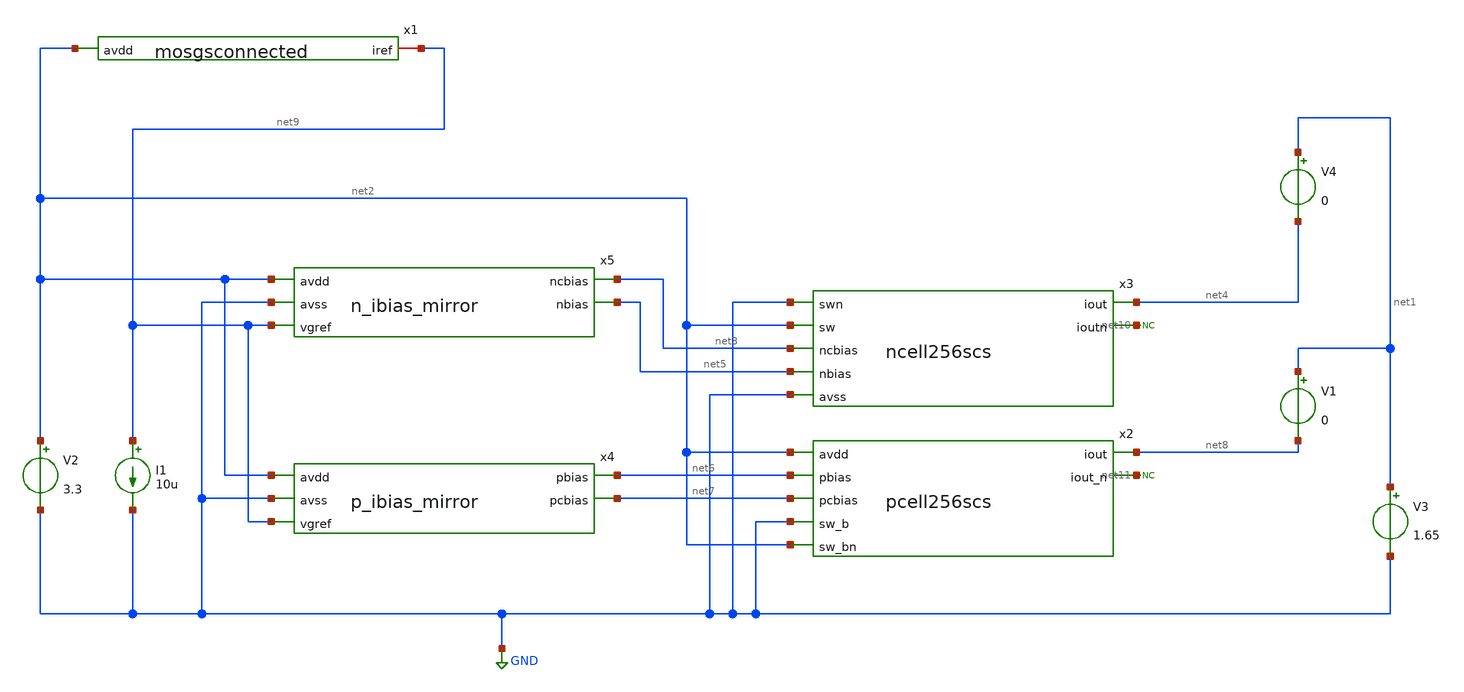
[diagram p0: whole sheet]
** sch_path: xschem/currentmirrors_tb.sch
**.subckt currentmirrors_tb
V2 net2 GND 3.3
V3 net1 GND 1.65
V4 net1 net4 0
I1 net9 GND 10u
V1 net1 net8 0
* noconn #net10
* noconn #net11
x1 net2 net9 mosgsconnected
x4 net2 net6 net9 net7 GND p_ibias_mirror
x5 net2 net9 net3 net5 GND n_ibias_mirror
x2 net2 net6 net7 GND net2 net11 net8 pcell256scs
x3 net4 net10 GND net2 net3 net5 GND ncell256scs
**** begin user architecture code
 .lib $::SKYWATER_MODELS/sky130.lib.spice ff

.param mc_mm_switch=0
.param mc_pr_switch=1



.option wnflag=0
.option savecurrents
.control
save all
dc v3 0 3.3 0.01
plot i(V4) i(V1)
write currentmirrortb.raw
op
.endc


**** end user architecture code
**.ends

* expanding   symbol:  mosgsconnected.sym # of pins=2
** sym_path: xschem/mosgsconnected.sym
** sch_path: xschem/mosgsconnected.sch
.subckt mosgsconnected avdd iref
*.ipin avdd
*.iopin iref
XM6 iref iref avdd avdd sky130_fd_pr__pfet_g5v0d10v5 L=1 W=12 nf=1 ad='int((nf+1)/2) * W/nf * 0.29' as='int((nf+2)/2) * W/nf * 0.29'
+ pd='2*int((nf+1)/2) * (W/nf + 0.29)' ps='2*int((nf+2)/2) * (W/nf + 0.29)' nrd='0.29 / W' nrs='0.29 / W'
+ sa=0 sb=0 sd=0 mult=1 m=1
.ends


* expanding   symbol:  p_ibias_mirror.sym # of pins=5
** sym_path: xschem/p_ibias_mirror.sym
** sch_path: xschem/p_ibias_mirror.sch
.subckt p_ibias_mirror avdd pbias vgref pcbias avss
*.ipin avdd
*.ipin avss
*.opin pbias
*.opin pcbias
*.ipin vgref
XM3 pcbias pcbias avdd avdd sky130_fd_pr__pfet_g5v0d10v5 L=12 W=8 nf=1 ad='int((nf+1)/2) * W/nf * 0.29'
+ as='int((nf+2)/2) * W/nf * 0.29' pd='2*int((nf+1)/2) * (W/nf + 0.29)' ps='2*int((nf+2)/2) * (W/nf + 0.29)'
+ nrd='0.29 / W' nrs='0.29 / W' sa=0 sb=0 sd=0 mult=1 m=1
XM4 net1 pbias avdd avdd sky130_fd_pr__pfet_g5v0d10v5 L=1 W=6 nf=1 ad='int((nf+1)/2) * W/nf * 0.29' as='int((nf+2)/2) * W/nf * 0.29'
+ pd='2*int((nf+1)/2) * (W/nf + 0.29)' ps='2*int((nf+2)/2) * (W/nf + 0.29)' nrd='0.29 / W' nrs='0.29 / W'
+ sa=0 sb=0 sd=0 mult=1 m=1
XM5 pbias pcbias net1 avdd sky130_fd_pr__pfet_g5v0d10v5 L=1 W=12 nf=1 ad='int((nf+1)/2) * W/nf * 0.29'
+ as='int((nf+2)/2) * W/nf * 0.29' pd='2*int((nf+1)/2) * (W/nf + 0.29)' ps='2*int((nf+2)/2) * (W/nf + 0.29)'
+ nrd='0.29 / W' nrs='0.29 / W' sa=0 sb=0 sd=0 mult=1 m=1
XM1 pbias net2 avss avss sky130_fd_pr__nfet_g5v0d10v5 L=1 W=7 nf=1 ad='int((nf+1)/2) * W/nf * 0.29' as='int((nf+2)/2) * W/nf * 0.29'
+ pd='2*int((nf+1)/2) * (W/nf + 0.29)' ps='2*int((nf+2)/2) * (W/nf + 0.29)' nrd='0.29 / W' nrs='0.29 / W'
+ sa=0 sb=0 sd=0 mult=1 m=1
XM2 net3 vgref avdd avdd sky130_fd_pr__pfet_g5v0d10v5 L=1 W=12 nf=1 ad='int((nf+1)/2) * W/nf * 0.29'
+ as='int((nf+2)/2) * W/nf * 0.29' pd='2*int((nf+1)/2) * (W/nf + 0.29)' ps='2*int((nf+2)/2) * (W/nf + 0.29)'
+ nrd='0.29 / W' nrs='0.29 / W' sa=0 sb=0 sd=0 mult=1 m=1
XM7 net2 net2 avss avss sky130_fd_pr__nfet_g5v0d10v5 L=1 W=10 nf=1 ad='int((nf+1)/2) * W/nf * 0.29' as='int((nf+2)/2) * W/nf * 0.29'
+ pd='2*int((nf+1)/2) * (W/nf + 0.29)' ps='2*int((nf+2)/2) * (W/nf + 0.29)' nrd='0.29 / W' nrs='0.29 / W'
+ sa=0 sb=0 sd=0 mult=1 m=1
XM8 pcbias net2 avss avss sky130_fd_pr__nfet_g5v0d10v5 L=1 W=7 nf=1 ad='int((nf+1)/2) * W/nf * 0.29'
+ as='int((nf+2)/2) * W/nf * 0.29' pd='2*int((nf+1)/2) * (W/nf + 0.29)' ps='2*int((nf+2)/2) * (W/nf + 0.29)'
+ nrd='0.29 / W' nrs='0.29 / W' sa=0 sb=0 sd=0 mult=1 m=1
XM9 net2 net2 net3 avdd sky130_fd_pr__pfet_g5v0d10v5 L=1 W=8 nf=1 ad='int((nf+1)/2) * W/nf * 0.29' as='int((nf+2)/2) * W/nf * 0.29'
+ pd='2*int((nf+1)/2) * (W/nf + 0.29)' ps='2*int((nf+2)/2) * (W/nf + 0.29)' nrd='0.29 / W' nrs='0.29 / W'
+ sa=0 sb=0 sd=0 mult=1 m=1
.ends


* expanding   symbol:  n_ibias_mirror.sym # of pins=5
** sym_path: xschem/n_ibias_mirror.sym
** sch_path: xschem/n_ibias_mirror.sch
.subckt n_ibias_mirror avdd vgref ncbias nbias avss
*.ipin avss
*.ipin avdd
*.opin nbias
*.opin ncbias
*.ipin vgref
XM1 net1 nbias avss avss sky130_fd_pr__nfet_g5v0d10v5 L=1 W=3 nf=1 ad='int((nf+1)/2) * W/nf * 0.29' as='int((nf+2)/2) * W/nf * 0.29'
+ pd='2*int((nf+1)/2) * (W/nf + 0.29)' ps='2*int((nf+2)/2) * (W/nf + 0.29)' nrd='0.29 / W' nrs='0.29 / W'
+ sa=0 sb=0 sd=0 mult=1 m=1
XM2 nbias ncbias net1 avss sky130_fd_pr__nfet_g5v0d10v5 L=1 W=6 nf=1 ad='int((nf+1)/2) * W/nf * 0.29'
+ as='int((nf+2)/2) * W/nf * 0.29' pd='2*int((nf+1)/2) * (W/nf + 0.29)' ps='2*int((nf+2)/2) * (W/nf + 0.29)'
+ nrd='0.29 / W' nrs='0.29 / W' sa=0 sb=0 sd=0 mult=1 m=1
XM3 ncbias ncbias avss avss sky130_fd_pr__nfet_g5v0d10v5 L=10 W=10 nf=1 ad='int((nf+1)/2) * W/nf * 0.29'
+ as='int((nf+2)/2) * W/nf * 0.29' pd='2*int((nf+1)/2) * (W/nf + 0.29)' ps='2*int((nf+2)/2) * (W/nf + 0.29)'
+ nrd='0.29 / W' nrs='0.29 / W' sa=0 sb=0 sd=0 mult=1 m=1
XM4 nbias vgref avdd avdd sky130_fd_pr__pfet_g5v0d10v5 L=1 W=7.5 nf=1 ad='int((nf+1)/2) * W/nf * 0.29'
+ as='int((nf+2)/2) * W/nf * 0.29' pd='2*int((nf+1)/2) * (W/nf + 0.29)' ps='2*int((nf+2)/2) * (W/nf + 0.29)'
+ nrd='0.29 / W' nrs='0.29 / W' sa=0 sb=0 sd=0 mult=1 m=1
XM5 ncbias vgref avdd avdd sky130_fd_pr__pfet_g5v0d10v5 L=1 W=7.5 nf=1 ad='int((nf+1)/2) * W/nf * 0.29'
+ as='int((nf+2)/2) * W/nf * 0.29' pd='2*int((nf+1)/2) * (W/nf + 0.29)' ps='2*int((nf+2)/2) * (W/nf + 0.29)'
+ nrd='0.29 / W' nrs='0.29 / W' sa=0 sb=0 sd=0 mult=1 m=1
.ends


* expanding   symbol:  pcell256scs.sym # of pins=7
** sym_path: xschem/pcell256scs.sym
** sch_path: xschem/pcell256scs.sch
.subckt pcell256scs avdd pbias pcbias sw_b sw_bn iout_n iout
*.ipin pbias
*.ipin pcbias
*.ipin sw_b
*.ipin avdd
*.opin iout
*.opin iout_n
*.ipin sw_bn
XM1 net1 pbias avdd avdd sky130_fd_pr__pfet_g5v0d10v5 L=1 W=6 nf=1 ad='int((nf+1)/2) * W/nf * 0.29' as='int((nf+2)/2) * W/nf * 0.29'
+ pd='2*int((nf+1)/2) * (W/nf + 0.29)' ps='2*int((nf+2)/2) * (W/nf + 0.29)' nrd='0.29 / W' nrs='0.29 / W'
+ sa=0 sb=0 sd=0 mult=256 m=256
XM2 net2 pcbias net1 avdd sky130_fd_pr__pfet_g5v0d10v5 L=1 W=12 nf=1 ad='int((nf+1)/2) * W/nf * 0.29'
+ as='int((nf+2)/2) * W/nf * 0.29' pd='2*int((nf+1)/2) * (W/nf + 0.29)' ps='2*int((nf+2)/2) * (W/nf + 0.29)'
+ nrd='0.29 / W' nrs='0.29 / W' sa=0 sb=0 sd=0 mult=256 m=256
XM3 iout sw_b net2 avdd sky130_fd_pr__pfet_g5v0d10v5 L=1 W=4 nf=1 ad='int((nf+1)/2) * W/nf * 0.29' as='int((nf+2)/2) * W/nf * 0.29'
+ pd='2*int((nf+1)/2) * (W/nf + 0.29)' ps='2*int((nf+2)/2) * (W/nf + 0.29)' nrd='0.29 / W' nrs='0.29 / W'
+ sa=0 sb=0 sd=0 mult=256 m=256
XM4 iout_n sw_bn net2 avdd sky130_fd_pr__pfet_g5v0d10v5 L=1 W=4 nf=1 ad='int((nf+1)/2) * W/nf * 0.29'
+ as='int((nf+2)/2) * W/nf * 0.29' pd='2*int((nf+1)/2) * (W/nf + 0.29)' ps='2*int((nf+2)/2) * (W/nf + 0.29)'
+ nrd='0.29 / W' nrs='0.29 / W' sa=0 sb=0 sd=0 mult=256 m=256
.ends


* expanding   symbol:  ncell256scs.sym # of pins=7
** sym_path: xschem/ncell256scs.sym
** sch_path: xschem/ncell256scs.sch
.subckt ncell256scs iout ioutn swn sw ncbias nbias avss
*.ipin sw
*.ipin ncbias
*.ipin nbias
*.ipin avss
*.opin iout
*.opin ioutn
*.ipin swn
XM8 net1 nbias avss avss sky130_fd_pr__nfet_g5v0d10v5 L=1 W=3 nf=1 ad='int((nf+1)/2) * W/nf * 0.29' as='int((nf+2)/2) * W/nf * 0.29'
+ pd='2*int((nf+1)/2) * (W/nf + 0.29)' ps='2*int((nf+2)/2) * (W/nf + 0.29)' nrd='0.29 / W' nrs='0.29 / W'
+ sa=0 sb=0 sd=0 mult=256 m=256
XM9 net2 ncbias net1 avss sky130_fd_pr__nfet_g5v0d10v5 L=1 W=6 nf=1 ad='int((nf+1)/2) * W/nf * 0.29'
+ as='int((nf+2)/2) * W/nf * 0.29' pd='2*int((nf+1)/2) * (W/nf + 0.29)' ps='2*int((nf+2)/2) * (W/nf + 0.29)'
+ nrd='0.29 / W' nrs='0.29 / W' sa=0 sb=0 sd=0 mult=256 m=256
XM1 iout sw net2 avss sky130_fd_pr__nfet_g5v0d10v5 L=1 W=6 nf=1 ad='int((nf+1)/2) * W/nf * 0.29' as='int((nf+2)/2) * W/nf * 0.29'
+ pd='2*int((nf+1)/2) * (W/nf + 0.29)' ps='2*int((nf+2)/2) * (W/nf + 0.29)' nrd='0.29 / W' nrs='0.29 / W'
+ sa=0 sb=0 sd=0 mult=256 m=256
XM2 ioutn swn net2 avss sky130_fd_pr__nfet_g5v0d10v5 L=1 W=6 nf=1 ad='int((nf+1)/2) * W/nf * 0.29' as='int((nf+2)/2) * W/nf * 0.29'
+ pd='2*int((nf+1)/2) * (W/nf + 0.29)' ps='2*int((nf+2)/2) * (W/nf + 0.29)' nrd='0.29 / W' nrs='0.29 / W'
+ sa=0 sb=0 sd=0 mult=256 m=256
.ends

.GLOBAL GND
.end
